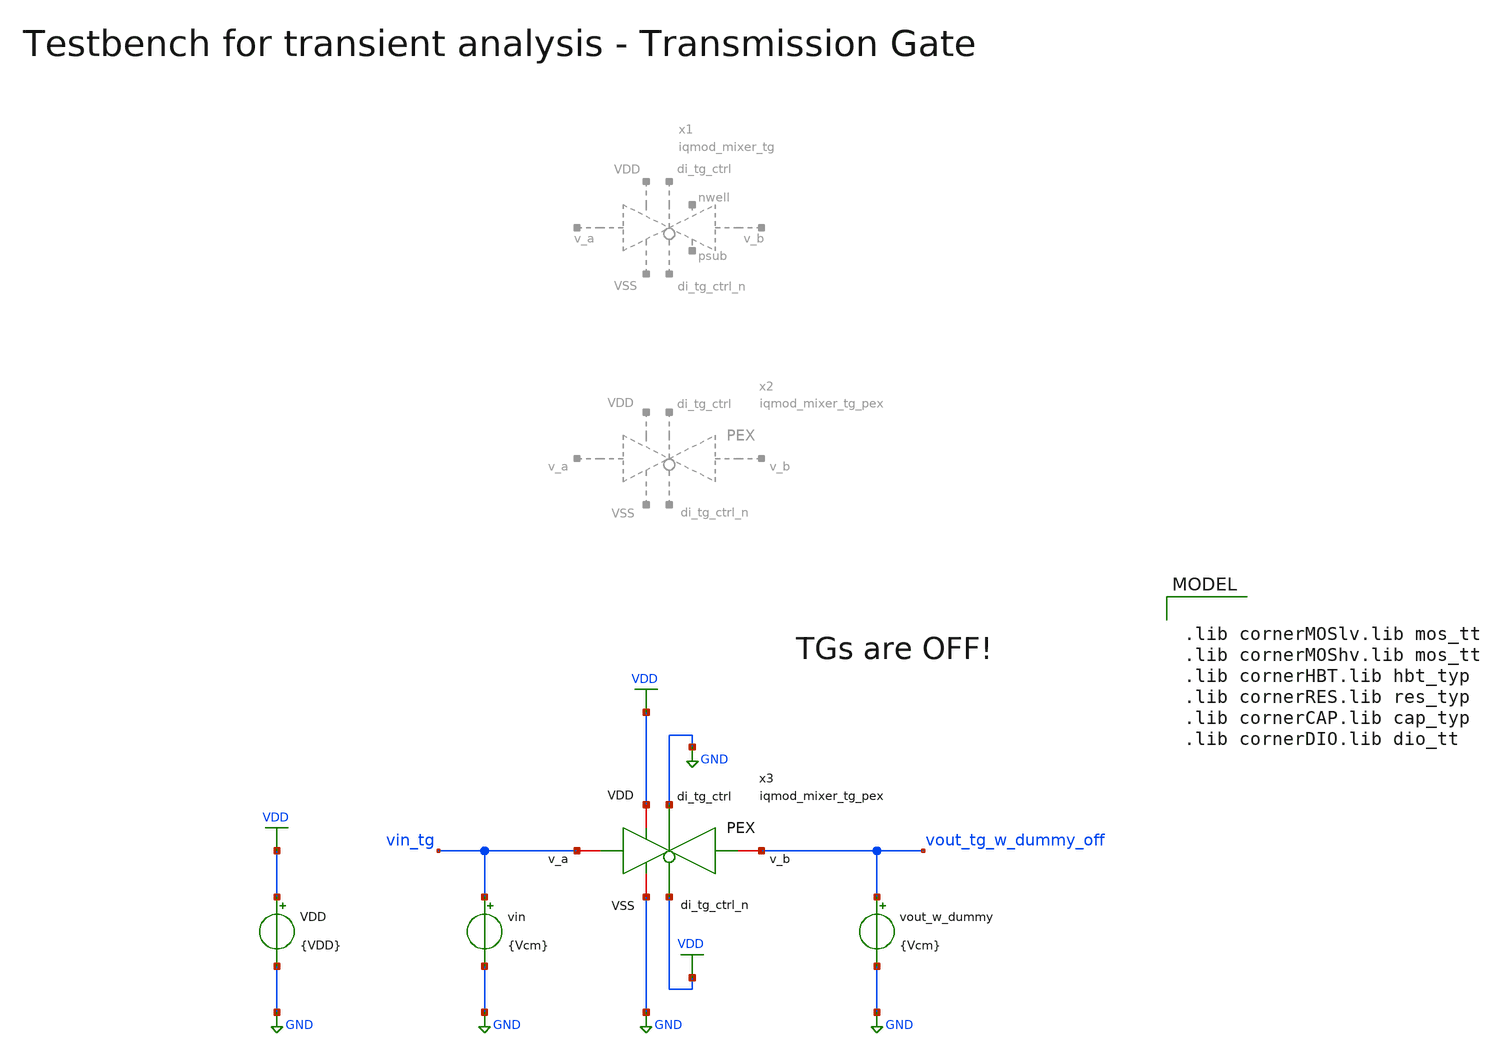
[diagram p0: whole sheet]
** sch_path: ihp130/macros/iqmod/xschem/testbenches/iqmod_mixer_tg_tb_dc_Ileak.sch
**.subckt iqmod_mixer_tg_tb_dc_Ileak
VDD VDD GND {VDD}
vin vin_tg GND {Vcm}
vout_w_dummy vout_tg_w_dummy_off GND {Vcm}
x3 VDD VDD GND GND vin_tg vout_tg_w_dummy_off iqmod_mixer_tg_pex
**** begin user architecture code


.include ../../verification/pex/iqmod_mixer_tg_pex.spice
.param VDD=1.5
.csparam VDD=VDD
.param Vcm=VDD/2
.csparam Vcm=Vcm
.param temp=27
.param Cload=10p
.options savecurrents klu method=gear reltol=1e-3 abstol=1e-15 gmin=1e-15
.control

save all

* Operating Point Analysis
op
remzerovec
write iqmod_mixer_tg_tb_dc_Ileak.raw
set appendwrite

* DC Sweep Analysis LV with Dummy
dc vin 0 $&VDD 10m vout_w_dummy 0 $&VDD $&Vcm
write iqmod_mixer_tg_tb_dc_Ileak.raw
set appendwrite

* Off-Leakage Current
let Ileak_w_dummy = i(vout_w_dummy)
plot Ileak_w_dummy

* Writing Data
set wr_singlescale
set wr_vecnames
let Ileak_w_dummy = dc1.Ileak_w_dummy
unset appendwrite
wrdata $PROJECT_PATH/python/plot_simulations/data/iqmod_mixer_tg_tb_dc_Ileak.txt v(Ileak_w_dummy)

*quit
.endc


.lib cornerMOSlv.lib mos_tt
.lib cornerMOShv.lib mos_tt
.lib cornerHBT.lib hbt_typ
.lib cornerRES.lib res_typ
.lib cornerCAP.lib cap_typ
.lib cornerDIO.lib dio_tt

**** end user architecture code
**.ends

* expanding   symbol:  iqmod_mixer_tg.sym # of pins=8
** sym_path: ihp130/macros/iqmod/xschem/iqmod_mixer_tg.sym
** sch_path: ihp130/macros/iqmod/xschem/iqmod_mixer_tg.sch
.subckt iqmod_mixer_tg nwell psub VDD di_tg_ctrl VSS v_b v_a di_tg_ctrl_n
*.iopin v_a
*.iopin v_b
*.ipin di_tg_ctrl
*.ipin di_tg_ctrl_n
*.iopin VDD
*.iopin VSS
*.iopin nwell
*.iopin psub
XM1 v_a di_tg_ctrl v_b psub sg13_lv_nmos w=108.0u l=0.13u ng=36 m=1 mm_ok=1
XM2 v_a di_tg_ctrl_n v_b nwell sg13_lv_pmos w=324.0u l=0.13u ng=36 m=1 mm_ok=1
XMdummy2 v_b di_tg_ctrl v_b nwell sg13_lv_pmos w=162.0u l=0.13u ng=18 m=1 mm_ok=1
XMdummy1 v_b di_tg_ctrl_n v_b psub sg13_lv_nmos w=54.0u l=0.13u ng=18 m=1 mm_ok=1
XR1 VDD nwell ntap1 R=2.829 w=29.86e-6 l=11.02e-6 rw=0.3e-6
XR2 VSS psub ptap1 R=3.29 w=29.86e-6 l=5.38e-6 rw=0.3e-6
.ends

.GLOBAL GND
.GLOBAL VDD
.end
